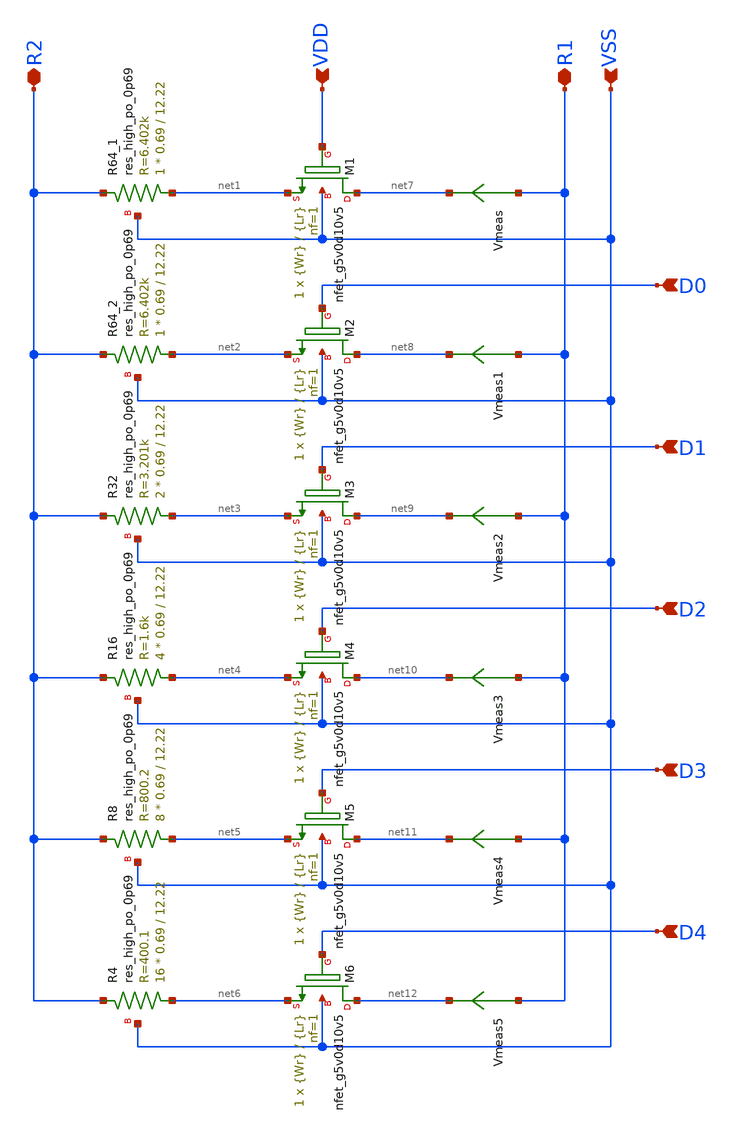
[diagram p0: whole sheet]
** sch_path: xschem/RA_array_v2.sch
**.subckt RA_array_v2 VSS R2 D0 D1 D2 D3 D4 R1 VDD
*.ipin VSS
*.iopin R2
*.ipin D0
*.ipin D1
*.ipin D2
*.ipin D3
*.ipin D4
*.iopin R1
*.ipin VDD
XM1 net7 VDD net1 VSS sky130_fd_pr__nfet_g5v0d10v5 L={Lr} W={Wr} nf=1 ad='int((nf+1)/2) * W/nf * 0.29'
+ as='int((nf+2)/2) * W/nf * 0.29' pd='2*int((nf+1)/2) * (W/nf + 0.29)' ps='2*int((nf+2)/2) * (W/nf + 0.29)'
+ nrd='0.29 / W' nrs='0.29 / W' sa=0 sb=0 sd=0 mult=1 m=1
XM2 net8 D0 net2 VSS sky130_fd_pr__nfet_g5v0d10v5 L={Lr} W={Wr} nf=1 ad='int((nf+1)/2) * W/nf * 0.29'
+ as='int((nf+2)/2) * W/nf * 0.29' pd='2*int((nf+1)/2) * (W/nf + 0.29)' ps='2*int((nf+2)/2) * (W/nf + 0.29)'
+ nrd='0.29 / W' nrs='0.29 / W' sa=0 sb=0 sd=0 mult=1 m=1
XM3 net9 D1 net3 VSS sky130_fd_pr__nfet_g5v0d10v5 L={Lr} W={Wr} nf=1 ad='int((nf+1)/2) * W/nf * 0.29'
+ as='int((nf+2)/2) * W/nf * 0.29' pd='2*int((nf+1)/2) * (W/nf + 0.29)' ps='2*int((nf+2)/2) * (W/nf + 0.29)'
+ nrd='0.29 / W' nrs='0.29 / W' sa=0 sb=0 sd=0 mult=1 m=1
XM4 net10 D2 net4 VSS sky130_fd_pr__nfet_g5v0d10v5 L={Lr} W={Wr} nf=1 ad='int((nf+1)/2) * W/nf * 0.29'
+ as='int((nf+2)/2) * W/nf * 0.29' pd='2*int((nf+1)/2) * (W/nf + 0.29)' ps='2*int((nf+2)/2) * (W/nf + 0.29)'
+ nrd='0.29 / W' nrs='0.29 / W' sa=0 sb=0 sd=0 mult=1 m=1
XM5 net11 D3 net5 VSS sky130_fd_pr__nfet_g5v0d10v5 L={Lr} W={Wr} nf=1 ad='int((nf+1)/2) * W/nf * 0.29'
+ as='int((nf+2)/2) * W/nf * 0.29' pd='2*int((nf+1)/2) * (W/nf + 0.29)' ps='2*int((nf+2)/2) * (W/nf + 0.29)'
+ nrd='0.29 / W' nrs='0.29 / W' sa=0 sb=0 sd=0 mult=1 m=1
XM6 net12 D4 net6 VSS sky130_fd_pr__nfet_g5v0d10v5 L={Lr} W={Wr} nf=1 ad='int((nf+1)/2) * W/nf * 0.29'
+ as='int((nf+2)/2) * W/nf * 0.29' pd='2*int((nf+1)/2) * (W/nf + 0.29)' ps='2*int((nf+2)/2) * (W/nf + 0.29)'
+ nrd='0.29 / W' nrs='0.29 / W' sa=0 sb=0 sd=0 mult=1 m=1
Vmeas R1 net7 0
.save i(vmeas)
Vmeas1 R1 net8 0
.save i(vmeas1)
Vmeas2 R1 net9 0
.save i(vmeas2)
Vmeas3 R1 net10 0
.save i(vmeas3)
Vmeas4 R1 net11 0
.save i(vmeas4)
Vmeas5 R1 net12 0
.save i(vmeas5)
XR64_1 net1 R2 VSS sky130_fd_pr__res_high_po_0p69 L=12.22 mult=1 m=1
XR32 net3 R2 VSS sky130_fd_pr__res_high_po_0p69 L=12.22 mult=2 m=2
XR16 net4 R2 VSS sky130_fd_pr__res_high_po_0p69 L=12.22 mult=4 m=4
XR8 net5 R2 VSS sky130_fd_pr__res_high_po_0p69 L=12.22 mult=8 m=8
XR4 net6 R2 VSS sky130_fd_pr__res_high_po_0p69 L=12.22 mult=16 m=16
XR64_2 net2 R2 VSS sky130_fd_pr__res_high_po_0p69 L=12.22 mult=1 m=1
**.ends
.end
